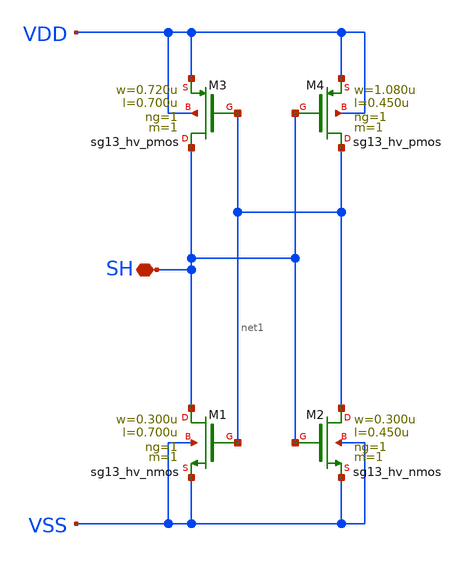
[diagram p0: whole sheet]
** sch_path: ihp-sg13g2/libs.ref/sg13g2_stdcell_hv/sch/xschem/sg13g2_hv_sighold.sch
* Copyright 2023 IHP PDK Authors
* Licensed under the Apache License, Version 2.0 (the "License");
* you may not use this file except in compliance with the License.
* You may obtain a copy of the License at
* https://www.apache.org/licenses/LICENSE-2.0
* Unless required by applicable law or agreed to in writing, software
* distributed under the License is distributed on an "AS IS" BASIS,
* WITHOUT WARRANTIES OR CONDITIONS OF ANY KIND, either express or implied.
* See the License for the specific language governing permissions and
* limitations under the License.
**.subckt sg13g2_hv_sighold SH
*.iopin SH
XM1 SH net1 VSS VSS sg13_hv_nmos w=0.300u l=0.700u ng=1 m=1 mm_ok=1
XM2 net1 SH VSS VSS sg13_hv_nmos w=0.300u l=0.450u ng=1 m=1 mm_ok=1
XM3 SH net1 VDD VDD sg13_hv_pmos w=0.720u l=0.700u ng=1 m=1 mm_ok=1
XM4 net1 SH VDD VDD sg13_hv_pmos w=1.080u l=0.450u ng=1 m=1 mm_ok=1
**.ends
.end
